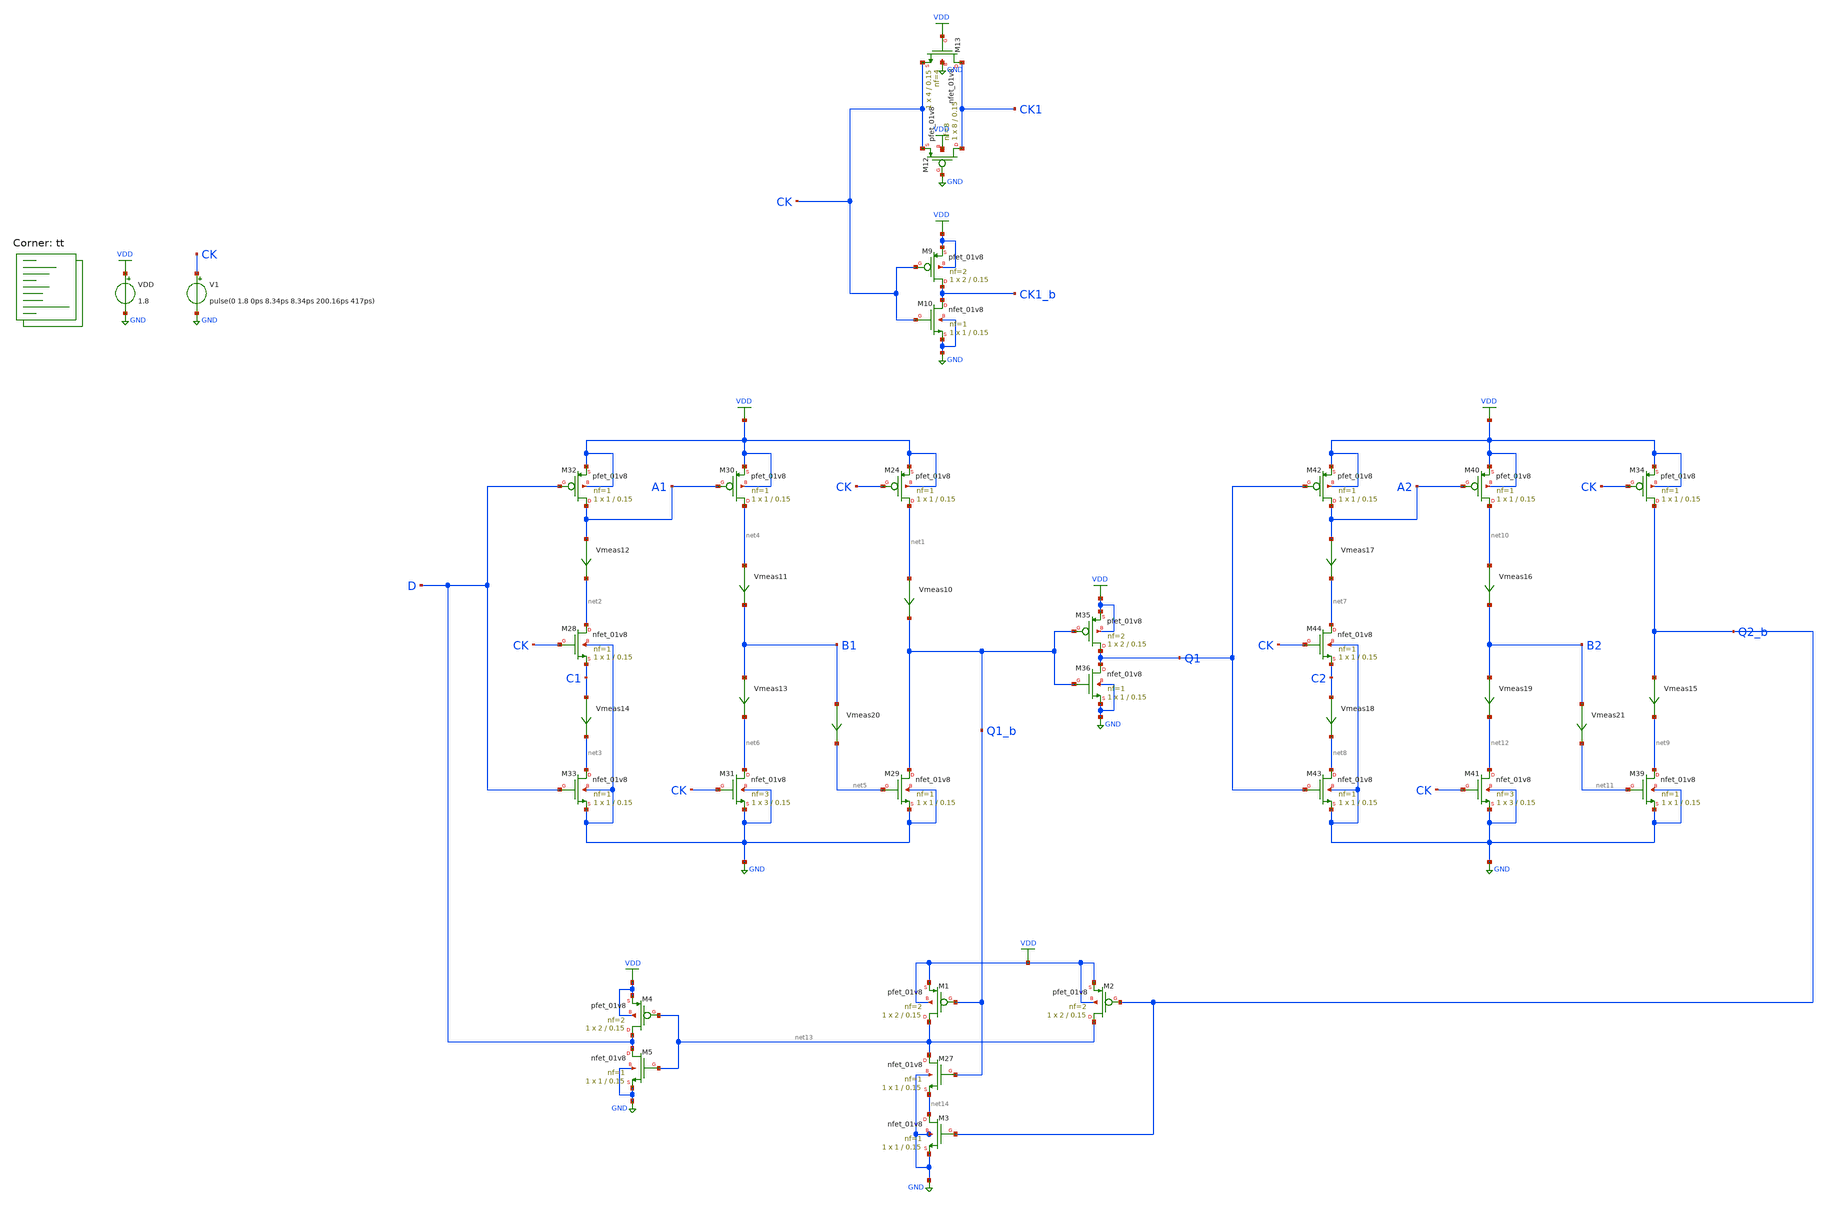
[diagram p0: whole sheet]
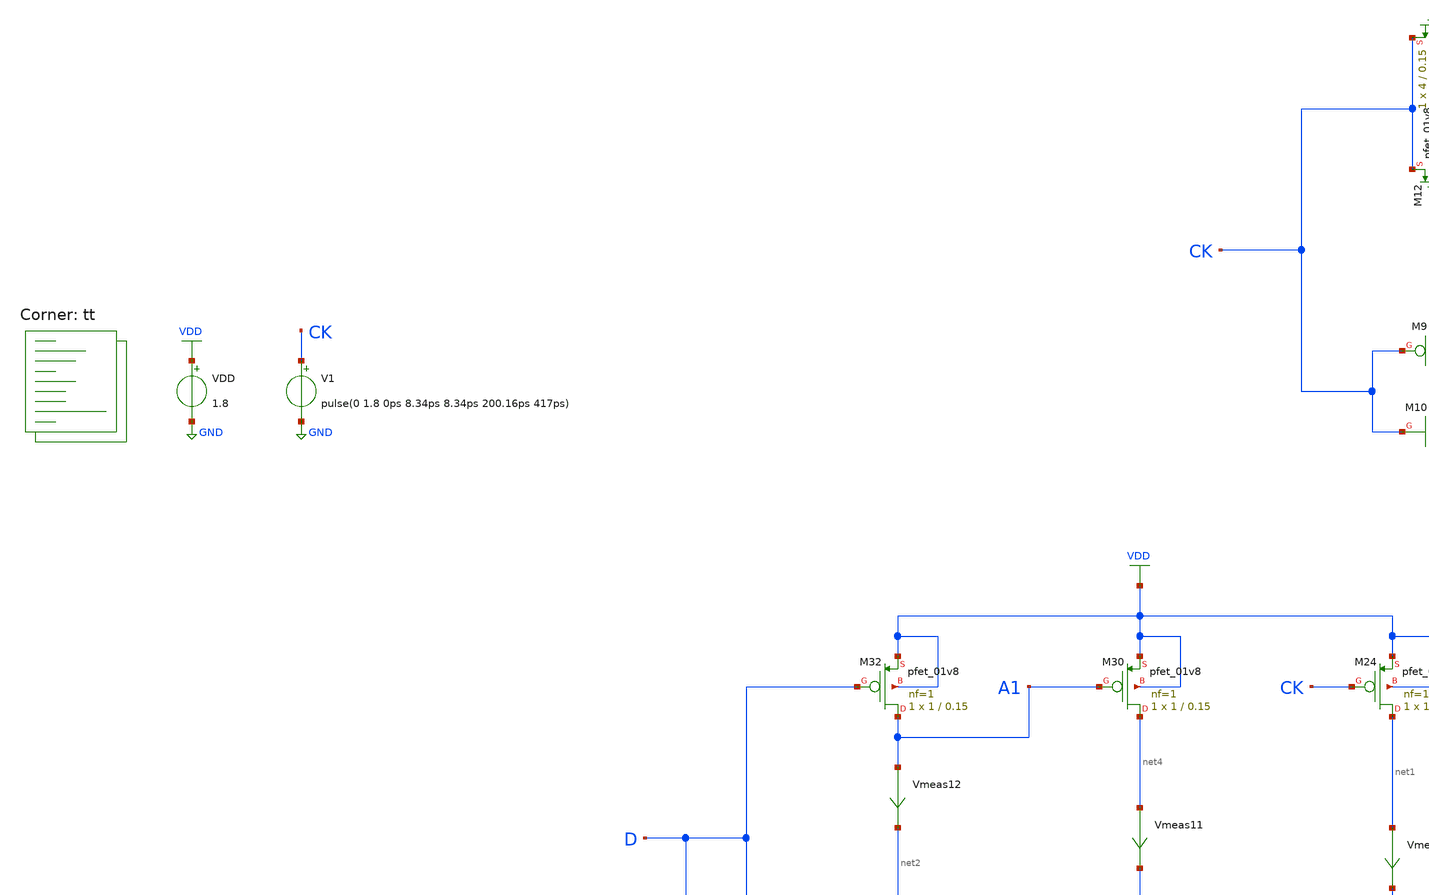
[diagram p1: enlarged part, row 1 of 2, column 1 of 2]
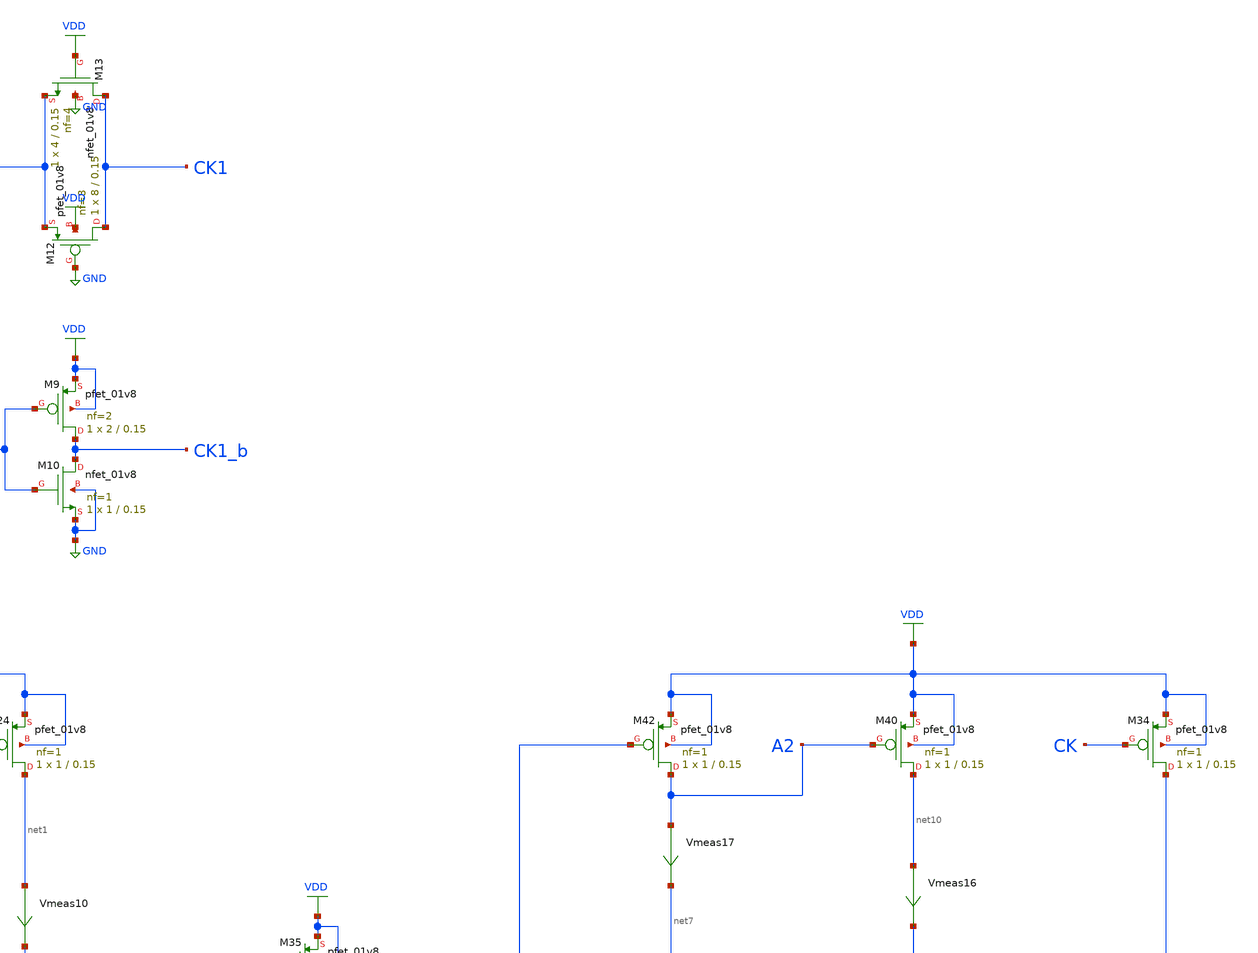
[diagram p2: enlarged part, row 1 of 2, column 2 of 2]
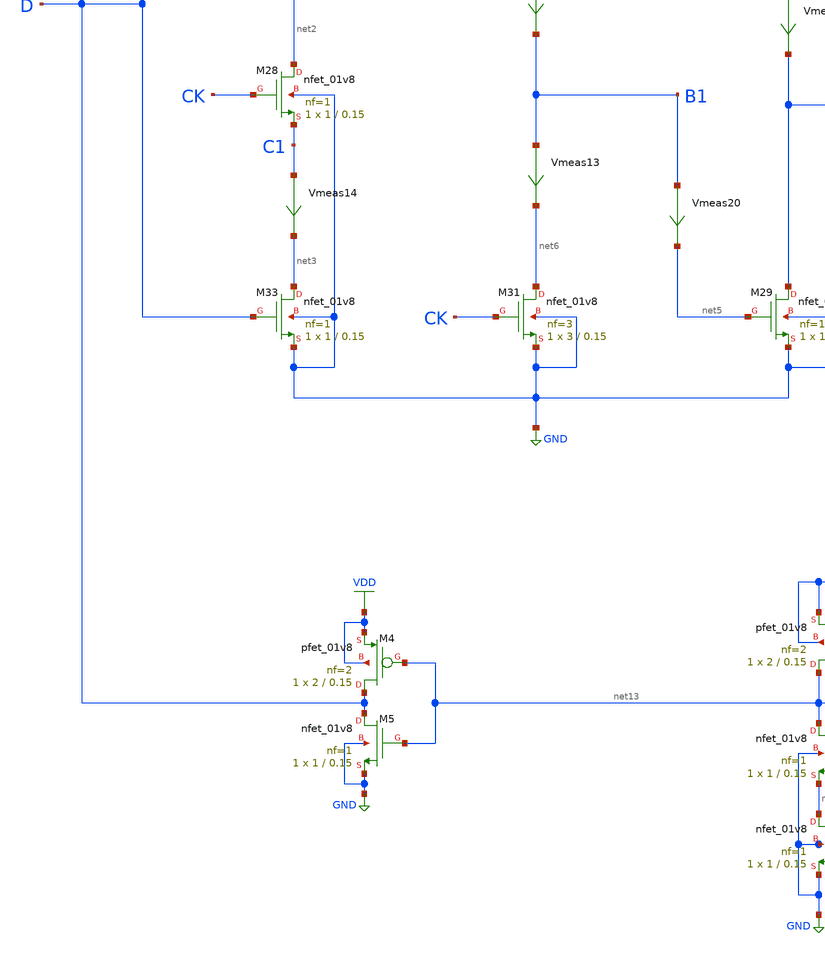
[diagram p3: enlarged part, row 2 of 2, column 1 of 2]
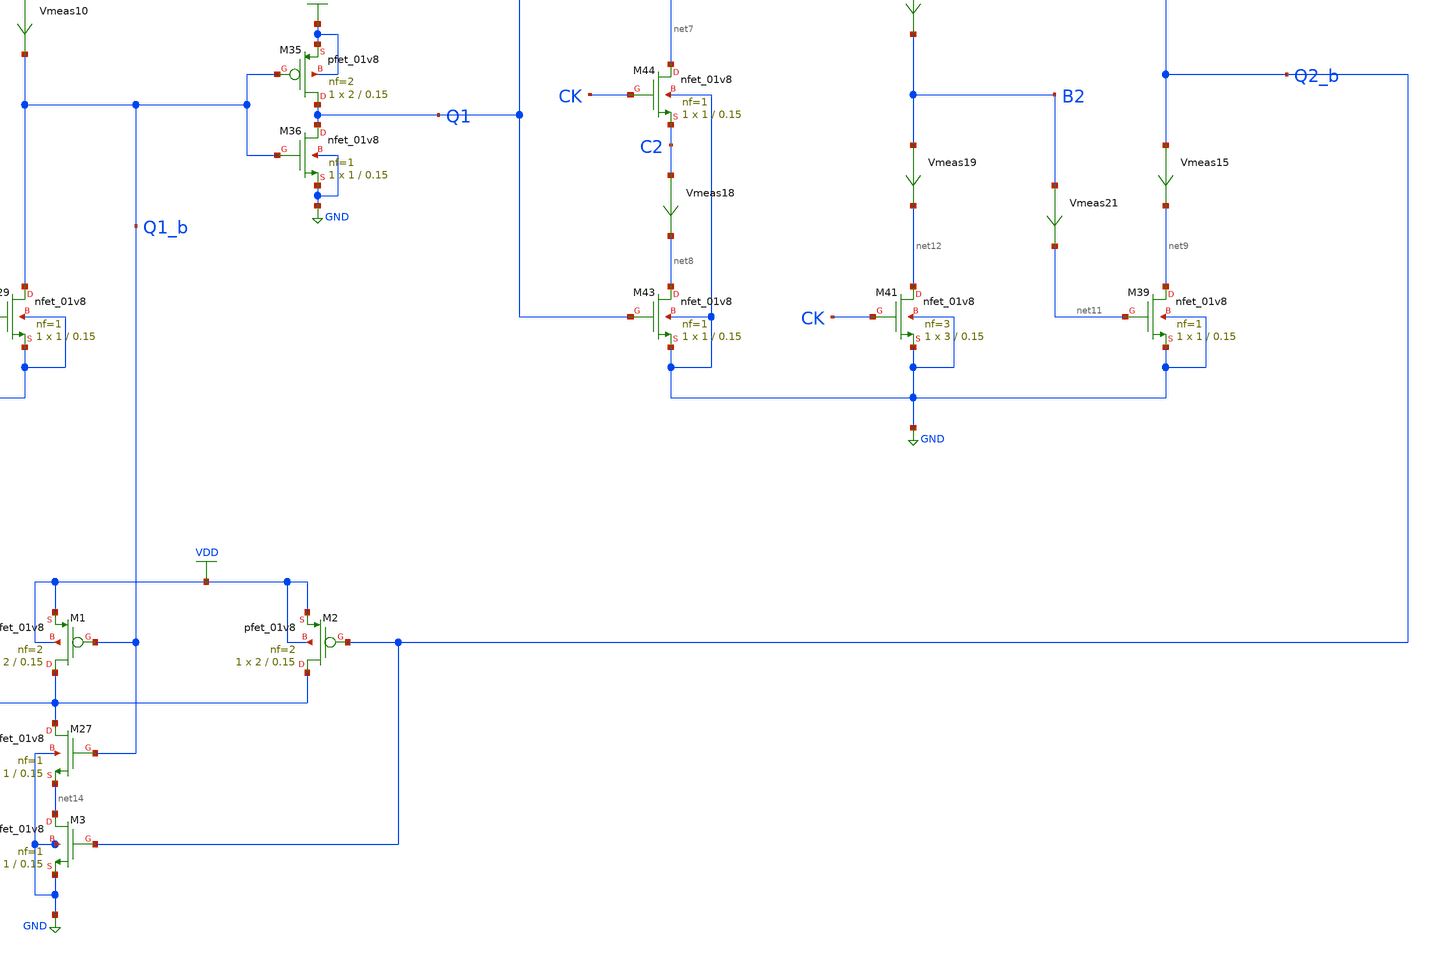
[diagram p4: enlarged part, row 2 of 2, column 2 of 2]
** sch_path: projects/pll/divider/xschem_ngspice/tb_TSPC_FF_ratioed_divide3.sch
**.subckt tb_TSPC_FF_ratioed_divide3
VDD VDD GND 1.8
XM12 CK1 GND CK VDD sky130_fd_pr__pfet_01v8 L=0.15 W=8 nf=8 ad='int((nf+1)/2) * W/nf * 0.29' as='int((nf+2)/2) * W/nf * 0.29'
+ pd='2*int((nf+1)/2) * (W/nf + 0.29)' ps='2*int((nf+2)/2) * (W/nf + 0.29)' nrd='0.29 / W' nrs='0.29 / W'
+ sa=0 sb=0 sd=0 mult=1 m=1
XM13 CK1 VDD CK GND sky130_fd_pr__nfet_01v8 L=0.15 W=4 nf=4 ad='int((nf+1)/2) * W/nf * 0.29' as='int((nf+2)/2) * W/nf * 0.29'
+ pd='2*int((nf+1)/2) * (W/nf + 0.29)' ps='2*int((nf+2)/2) * (W/nf + 0.29)' nrd='0.29 / W' nrs='0.29 / W'
+ sa=0 sb=0 sd=0 mult=1 m=1
XM9 CK1_b CK VDD VDD sky130_fd_pr__pfet_01v8 L=0.15 W=2 nf=2 ad='int((nf+1)/2) * W/nf * 0.29' as='int((nf+2)/2) * W/nf * 0.29'
+ pd='2*int((nf+1)/2) * (W/nf + 0.29)' ps='2*int((nf+2)/2) * (W/nf + 0.29)' nrd='0.29 / W' nrs='0.29 / W'
+ sa=0 sb=0 sd=0 mult=1 m=1
XM10 CK1_b CK GND GND sky130_fd_pr__nfet_01v8 L=0.15 W=1 nf=1 ad='int((nf+1)/2) * W/nf * 0.29' as='int((nf+2)/2) * W/nf * 0.29'
+ pd='2*int((nf+1)/2) * (W/nf + 0.29)' ps='2*int((nf+2)/2) * (W/nf + 0.29)' nrd='0.29 / W' nrs='0.29 / W'
+ sa=0 sb=0 sd=0 mult=1 m=1
XM24 net1 CK VDD VDD sky130_fd_pr__pfet_01v8 L=0.15 W=1 nf=1 ad='int((nf+1)/2) * W/nf * 0.29' as='int((nf+2)/2) * W/nf * 0.29'
+ pd='2*int((nf+1)/2) * (W/nf + 0.29)' ps='2*int((nf+2)/2) * (W/nf + 0.29)' nrd='0.29 / W' nrs='0.29 / W'
+ sa=0 sb=0 sd=0 mult=1 m=1
Vmeas10 net1 Q1_b 0
.save i(vmeas10)
XM29 Q1_b net5 GND GND sky130_fd_pr__nfet_01v8 L=0.15 W=1 nf=1 ad='int((nf+1)/2) * W/nf * 0.29' as='int((nf+2)/2) * W/nf * 0.29'
+ pd='2*int((nf+1)/2) * (W/nf + 0.29)' ps='2*int((nf+2)/2) * (W/nf + 0.29)' nrd='0.29 / W' nrs='0.29 / W'
+ sa=0 sb=0 sd=0 mult=1 m=1
XM30 net4 A1 VDD VDD sky130_fd_pr__pfet_01v8 L=0.15 W=1 nf=1 ad='int((nf+1)/2) * W/nf * 0.29' as='int((nf+2)/2) * W/nf * 0.29'
+ pd='2*int((nf+1)/2) * (W/nf + 0.29)' ps='2*int((nf+2)/2) * (W/nf + 0.29)' nrd='0.29 / W' nrs='0.29 / W'
+ sa=0 sb=0 sd=0 mult=1 m=1
XM31 net6 CK GND GND sky130_fd_pr__nfet_01v8 L=0.15 W=3 nf=3 ad='int((nf+1)/2) * W/nf * 0.29' as='int((nf+2)/2) * W/nf * 0.29'
+ pd='2*int((nf+1)/2) * (W/nf + 0.29)' ps='2*int((nf+2)/2) * (W/nf + 0.29)' nrd='0.29 / W' nrs='0.29 / W'
+ sa=0 sb=0 sd=0 mult=1 m=1
Vmeas11 net4 B1 0
.save i(vmeas11)
XM32 A1 D VDD VDD sky130_fd_pr__pfet_01v8 L=0.15 W=1 nf=1 ad='int((nf+1)/2) * W/nf * 0.29' as='int((nf+2)/2) * W/nf * 0.29'
+ pd='2*int((nf+1)/2) * (W/nf + 0.29)' ps='2*int((nf+2)/2) * (W/nf + 0.29)' nrd='0.29 / W' nrs='0.29 / W'
+ sa=0 sb=0 sd=0 mult=1 m=1
XM33 net3 D GND GND sky130_fd_pr__nfet_01v8 L=0.15 W=1 nf=1 ad='int((nf+1)/2) * W/nf * 0.29' as='int((nf+2)/2) * W/nf * 0.29'
+ pd='2*int((nf+1)/2) * (W/nf + 0.29)' ps='2*int((nf+2)/2) * (W/nf + 0.29)' nrd='0.29 / W' nrs='0.29 / W'
+ sa=0 sb=0 sd=0 mult=1 m=1
Vmeas12 A1 net2 0
.save i(vmeas12)
Vmeas14 C1 net3 0
.save i(vmeas14)
XM28 net2 CK C1 GND sky130_fd_pr__nfet_01v8 L=0.15 W=1 nf=1 ad='int((nf+1)/2) * W/nf * 0.29' as='int((nf+2)/2) * W/nf * 0.29'
+ pd='2*int((nf+1)/2) * (W/nf + 0.29)' ps='2*int((nf+2)/2) * (W/nf + 0.29)' nrd='0.29 / W' nrs='0.29 / W'
+ sa=0 sb=0 sd=0 mult=1 m=1
Vmeas13 B1 net6 0
.save i(vmeas13)
Vmeas20 B1 net5 0
.save i(vmeas20)
XM34 Q2_b CK VDD VDD sky130_fd_pr__pfet_01v8 L=0.15 W=1 nf=1 ad='int((nf+1)/2) * W/nf * 0.29' as='int((nf+2)/2) * W/nf * 0.29'
+ pd='2*int((nf+1)/2) * (W/nf + 0.29)' ps='2*int((nf+2)/2) * (W/nf + 0.29)' nrd='0.29 / W' nrs='0.29 / W'
+ sa=0 sb=0 sd=0 mult=1 m=1
Vmeas15 Q2_b net9 0
.save i(vmeas15)
XM39 net9 net11 GND GND sky130_fd_pr__nfet_01v8 L=0.15 W=1 nf=1 ad='int((nf+1)/2) * W/nf * 0.29' as='int((nf+2)/2) * W/nf * 0.29'
+ pd='2*int((nf+1)/2) * (W/nf + 0.29)' ps='2*int((nf+2)/2) * (W/nf + 0.29)' nrd='0.29 / W' nrs='0.29 / W'
+ sa=0 sb=0 sd=0 mult=1 m=1
XM40 net10 A2 VDD VDD sky130_fd_pr__pfet_01v8 L=0.15 W=1 nf=1 ad='int((nf+1)/2) * W/nf * 0.29' as='int((nf+2)/2) * W/nf * 0.29'
+ pd='2*int((nf+1)/2) * (W/nf + 0.29)' ps='2*int((nf+2)/2) * (W/nf + 0.29)' nrd='0.29 / W' nrs='0.29 / W'
+ sa=0 sb=0 sd=0 mult=1 m=1
XM41 net12 CK GND GND sky130_fd_pr__nfet_01v8 L=0.15 W=3 nf=3 ad='int((nf+1)/2) * W/nf * 0.29' as='int((nf+2)/2) * W/nf * 0.29'
+ pd='2*int((nf+1)/2) * (W/nf + 0.29)' ps='2*int((nf+2)/2) * (W/nf + 0.29)' nrd='0.29 / W' nrs='0.29 / W'
+ sa=0 sb=0 sd=0 mult=1 m=1
Vmeas16 net10 B2 0
.save i(vmeas16)
XM42 A2 Q1 VDD VDD sky130_fd_pr__pfet_01v8 L=0.15 W=1 nf=1 ad='int((nf+1)/2) * W/nf * 0.29' as='int((nf+2)/2) * W/nf * 0.29'
+ pd='2*int((nf+1)/2) * (W/nf + 0.29)' ps='2*int((nf+2)/2) * (W/nf + 0.29)' nrd='0.29 / W' nrs='0.29 / W'
+ sa=0 sb=0 sd=0 mult=1 m=1
XM43 net8 Q1 GND GND sky130_fd_pr__nfet_01v8 L=0.15 W=1 nf=1 ad='int((nf+1)/2) * W/nf * 0.29' as='int((nf+2)/2) * W/nf * 0.29'
+ pd='2*int((nf+1)/2) * (W/nf + 0.29)' ps='2*int((nf+2)/2) * (W/nf + 0.29)' nrd='0.29 / W' nrs='0.29 / W'
+ sa=0 sb=0 sd=0 mult=1 m=1
Vmeas17 A2 net7 0
.save i(vmeas17)
Vmeas18 C2 net8 0
.save i(vmeas18)
XM44 net7 CK C2 GND sky130_fd_pr__nfet_01v8 L=0.15 W=1 nf=1 ad='int((nf+1)/2) * W/nf * 0.29' as='int((nf+2)/2) * W/nf * 0.29'
+ pd='2*int((nf+1)/2) * (W/nf + 0.29)' ps='2*int((nf+2)/2) * (W/nf + 0.29)' nrd='0.29 / W' nrs='0.29 / W'
+ sa=0 sb=0 sd=0 mult=1 m=1
Vmeas19 B2 net12 0
.save i(vmeas19)
Vmeas21 B2 net11 0
.save i(vmeas21)
V1 CK GND pulse(0 1.8 0ps 8.34ps 8.34ps 200.16ps 417ps)
XM35 Q1 Q1_b VDD VDD sky130_fd_pr__pfet_01v8 L=0.15 W=2 nf=2 ad='int((nf+1)/2) * W/nf * 0.29' as='int((nf+2)/2) * W/nf * 0.29'
+ pd='2*int((nf+1)/2) * (W/nf + 0.29)' ps='2*int((nf+2)/2) * (W/nf + 0.29)' nrd='0.29 / W' nrs='0.29 / W'
+ sa=0 sb=0 sd=0 mult=1 m=1
XM36 Q1 Q1_b GND GND sky130_fd_pr__nfet_01v8 L=0.15 W=1 nf=1 ad='int((nf+1)/2) * W/nf * 0.29' as='int((nf+2)/2) * W/nf * 0.29'
+ pd='2*int((nf+1)/2) * (W/nf + 0.29)' ps='2*int((nf+2)/2) * (W/nf + 0.29)' nrd='0.29 / W' nrs='0.29 / W'
+ sa=0 sb=0 sd=0 mult=1 m=1
XM27 net13 Q1_b net14 GND sky130_fd_pr__nfet_01v8 L=0.15 W=1 nf=1 ad='int((nf+1)/2) * W/nf * 0.29' as='int((nf+2)/2) * W/nf * 0.29'
+ pd='2*int((nf+1)/2) * (W/nf + 0.29)' ps='2*int((nf+2)/2) * (W/nf + 0.29)' nrd='0.29 / W' nrs='0.29 / W'
+ sa=0 sb=0 sd=0 mult=1 m=1
XM1 net13 Q1_b VDD VDD sky130_fd_pr__pfet_01v8 L=0.15 W=2 nf=2 ad='int((nf+1)/2) * W/nf * 0.29' as='int((nf+2)/2) * W/nf * 0.29'
+ pd='2*int((nf+1)/2) * (W/nf + 0.29)' ps='2*int((nf+2)/2) * (W/nf + 0.29)' nrd='0.29 / W' nrs='0.29 / W'
+ sa=0 sb=0 sd=0 mult=1 m=1
XM2 net13 Q2_b VDD VDD sky130_fd_pr__pfet_01v8 L=0.15 W=2 nf=2 ad='int((nf+1)/2) * W/nf * 0.29' as='int((nf+2)/2) * W/nf * 0.29'
+ pd='2*int((nf+1)/2) * (W/nf + 0.29)' ps='2*int((nf+2)/2) * (W/nf + 0.29)' nrd='0.29 / W' nrs='0.29 / W'
+ sa=0 sb=0 sd=0 mult=1 m=1
XM3 net14 Q2_b GND GND sky130_fd_pr__nfet_01v8 L=0.15 W=1 nf=1 ad='int((nf+1)/2) * W/nf * 0.29' as='int((nf+2)/2) * W/nf * 0.29'
+ pd='2*int((nf+1)/2) * (W/nf + 0.29)' ps='2*int((nf+2)/2) * (W/nf + 0.29)' nrd='0.29 / W' nrs='0.29 / W'
+ sa=0 sb=0 sd=0 mult=1 m=1
XM4 D net13 VDD VDD sky130_fd_pr__pfet_01v8 L=0.15 W=2 nf=2 ad='int((nf+1)/2) * W/nf * 0.29' as='int((nf+2)/2) * W/nf * 0.29'
+ pd='2*int((nf+1)/2) * (W/nf + 0.29)' ps='2*int((nf+2)/2) * (W/nf + 0.29)' nrd='0.29 / W' nrs='0.29 / W'
+ sa=0 sb=0 sd=0 mult=1 m=1
XM5 D net13 GND GND sky130_fd_pr__nfet_01v8 L=0.15 W=1 nf=1 ad='int((nf+1)/2) * W/nf * 0.29' as='int((nf+2)/2) * W/nf * 0.29'
+ pd='2*int((nf+1)/2) * (W/nf + 0.29)' ps='2*int((nf+2)/2) * (W/nf + 0.29)' nrd='0.29 / W' nrs='0.29 / W'
+ sa=0 sb=0 sd=0 mult=1 m=1
**** begin user architecture code



.include /foss/pdks/sky130A/libs.ref/sky130_fd_sc_hd/spice/sky130_fd_sc_hd.spice

.option method=gear
.option wnflag=1
.option savecurrents


*.ic v(d)=0
*.ic v(q)=0
*.ic v(q1)=0

.control

  save v(d) v(q1) v(q1_b) v(q2_b) v(a1) v(a2) v(a3) v(a4) v(b1) v(b2) v(c1) v(c2) v(ck) v(ck1)
+ v(ck1_b)
  * save all
  * tran 0.1n 1u
  tran 1p 20n

  remzerovec
  write tb_TSPC_FF_ratioed_divide3.raw
  * set appendwrite

.endc



.lib $::SKYWATER_MODELS/sky130.lib.spice tt
**** end user architecture code
**.ends
.GLOBAL GND
.GLOBAL VDD
.end
